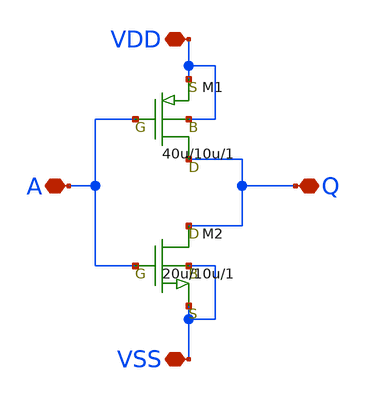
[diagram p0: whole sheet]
** sch_path: member_project/Takuzen/xscheme-klayout-initial/inverter.sch
**.subckt inverter A VDD Q VSS
*.iopin A
*.iopin VDD
*.iopin Q
*.iopin VSS
M1 Q A VDD VDD pch w=40u l=10u as=0 ps=0 ad=0 pd=0 m=1
M2 Q A VSS VSS nch w=20u l=10u as=0 ps=0 ad=0 pd=0 m=1
**.ends
.end
